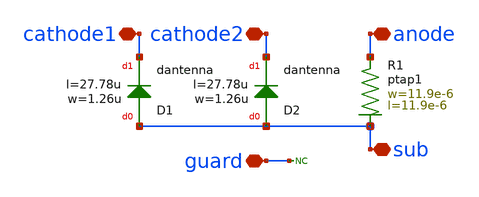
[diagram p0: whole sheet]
** sch_path: ihp-sg13cmos5l/libs.tech/xschem/hm_stdcells/sg13cmos5l_DCNDiode.sch
**.subckt sg13cmos5l_DCNDiode cathode2 guard anode cathode1 sub
*.iopin cathode2
*.iopin guard
*.iopin anode
*.iopin cathode1
*.iopin sub
XD1 sub cathode1 dantenna l=27.78u w=1.26u
* noconn guard
XD2 sub cathode2 dantenna l=27.78u w=1.26u
XR1 anode sub ptap1 R=5.179 w=11.9e-6 l=11.9e-6
**.ends
.end
